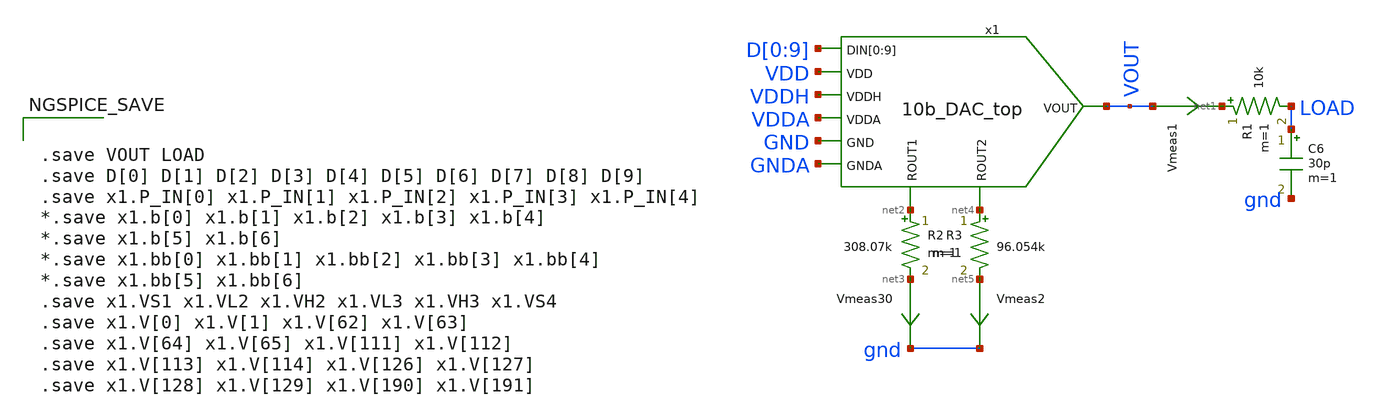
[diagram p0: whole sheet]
** sch_path: xschem/10b_DAC-tb.sch
.lib $::SKYWATER_MODELS/sky130.lib.spice tt
.include $::SKYWATER_STDCELLS/sky130_fd_sc_hd.spice

**.subckt 10b_DAC-tb
C6 LOAD gnd 30p m=1
R1 net1 LOAD 10k m=1
Vmeas1 VOUT net1 0
.save i(vmeas1)
R2 net2 net3 308.07k m=1
Vmeas30 net3 gnd 0
.save i(vmeas30)
R3 net4 net5 96.054k m=1
Vmeas2 net5 gnd 0
.save i(vmeas2)
x1 D[0] D[1] D[2] D[3] D[4] D[5] D[6] D[7] D[8] D[9] VDD VDDH VDDA GND GNDA VOUT net2 net4
+ 10b_DAC_top
**** begin user architecture code



  .option wnflag=1
  .option safecurrents
  .option klu
  ********************Static Voltage Sources***************************
  Vddh vddh gnd dc 5.5
  Vdd vdd gnd dc 1.8
  Vdda vdda gnd dc 5.5
  Vgnda gnda gnd dc 0
  ********************Dynamic Voltage Sources***************************
  *******Calculation**********
  .param base_f=50e3 base_t={1/base_f} base_th={base_t/2} base_d={base_th}
  .param d0_th={base_th} d0_t={d0_th*2}
  .param d1_th={d0_th*2} d1_t={d1_th*2}
  .param d2_th={d1_th*2} d2_t={d2_th*2}
  .param d3_th={d2_th*2} d3_t={d3_th*2}
  .param d4_th={d3_th*2} d4_t={d4_th*2}
  .param d5_th={d4_th*2} d5_t={d5_th*2}
  .param d6_th={d5_th*2} d6_t={d6_th*2}
  .param d7_th={d6_th*2} d7_t={d7_th*2}
  .param d8_th={d7_th*2} d8_t={d8_th*2}
  .param d9_th={d8_th*2} d9_t={d9_th*2}
  *******Signals**********
  .param vhi=1.8
  Vd0  d[0]  gnd pulse({vhi} 0 {base_d} 1n 1n {d0_th} {d0_t})
  Vd1  d[1]  gnd pulse({vhi} 0 {base_d} 1n 1n {d1_th} {d1_t})
  Vd2  d[2]  gnd pulse({vhi} 0 {base_d} 1n 1n {d2_th} {d2_t})
  Vd3  d[3]  gnd pulse({vhi} 0 {base_d} 1n 1n {d3_th} {d3_t})
  Vd4  d[4]  gnd pulse({vhi} 0 {base_d} 1n 1n {d4_th} {d4_t})
  Vd5  d[5]  gnd pulse({vhi} 0 {base_d} 1n 1n {d5_th} {d5_t})
  Vd6  d[6]  gnd pulse({vhi} 0 {base_d} 1n 1n {d6_th} {d6_t})
  Vd7  d[7]  gnd pulse({vhi} 0 {base_d} 1n 1n {d7_th} {d7_t})
  Vd8  d[8]  gnd pulse({vhi} 0 {base_d} 1n 1n {d8_th} {d8_t})
  Vd9  d[9]  gnd pulse({vhi} 0 {base_d} 1n 1n {d9_th} {d9_t})

  *Vd6  d[6]  gnd 0
  *Vd7  d[7]  gnd 0
  *Vd8  d[8]  gnd 0
  *Vd9  d[9]  gnd 0
  ********************Simulation Commands*****************************
  .control
     reset
     set num_threads=30
     tran 1n 1m
     write 10b_DAC-tb.raw

     set wr_vecnames
     set wr_singlescale
     wrdata /home/yohanes/10-bit-DAC/simulations/top-tb.txt VOUT LOAD D[0] D[1] D[2] D[3] D[4] D[5]
+ D[6] D[7] D[8] D[9]

*    quit 0
  .endc





.save VOUT LOAD
.save D[0] D[1] D[2] D[3] D[4] D[5] D[6] D[7] D[8] D[9]
.save x1.P_IN[0] x1.P_IN[1] x1.P_IN[2] x1.P_IN[3] x1.P_IN[4]
*.save x1.b[0] x1.b[1] x1.b[2] x1.b[3] x1.b[4]
*.save x1.b[5] x1.b[6]
*.save x1.bb[0] x1.bb[1] x1.bb[2] x1.bb[3] x1.bb[4]
*.save x1.bb[5] x1.bb[6]
.save x1.VS1 x1.VL2 x1.VH2 x1.VL3 x1.VH3 x1.VS4
.save x1.V[0] x1.V[1] x1.V[62] x1.V[63]
.save x1.V[64] x1.V[65] x1.V[111] x1.V[112]
.save x1.V[113] x1.V[114] x1.V[126] x1.V[127]
.save x1.V[128] x1.V[129] x1.V[190] x1.V[191]


**** end user architecture code
**.ends
.end
